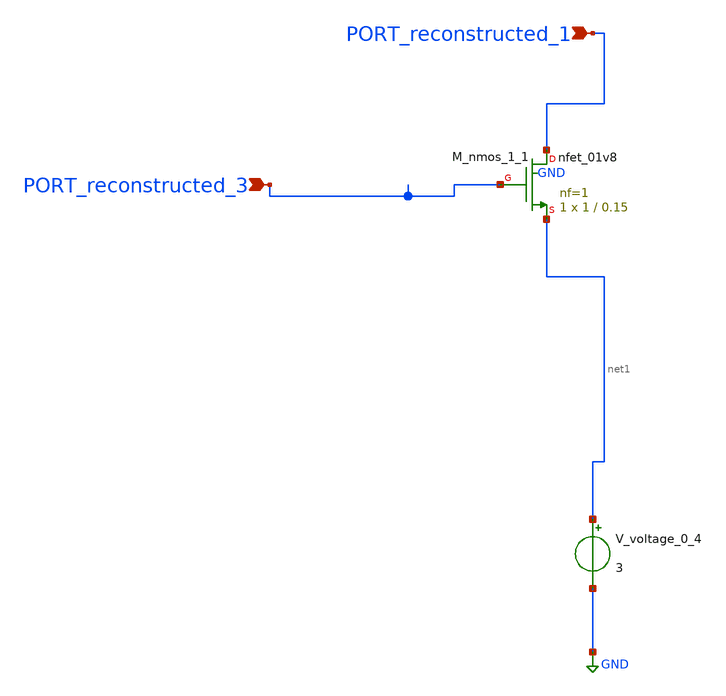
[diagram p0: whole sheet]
** sch_path: schematics/AMSNet/17.sch
**.subckt 17 PORT_reconstructed_3 PORT_reconstructed_1
*.ipin PORT_reconstructed_3
*.ipin PORT_reconstructed_1
XM_nmos_1_1 PORT_reconstructed_1 PORT_reconstructed_3 net1 GND sky130_fd_pr__nfet_01v8 L=0.15 W=1 nf=1
+ ad='int((1 + 1)/2) * 1 / 1 * 0.29' as='int((1 + 2)/2) * 1 / 1 * 0.29' pd='2*int((1 + 1)/2) * (1 / 1 + 0.29)'
+ ps='2*int((1 + 2)/2) * (1 / 1 + 0.29)' nrd='0.29 / 1 ' nrs='0.29 / 1 ' sa=0 sb=0 sd=0 mult=1 m=1
V_voltage_0_4 net1 GND 3
**.ends
.GLOBAL GND
.end
